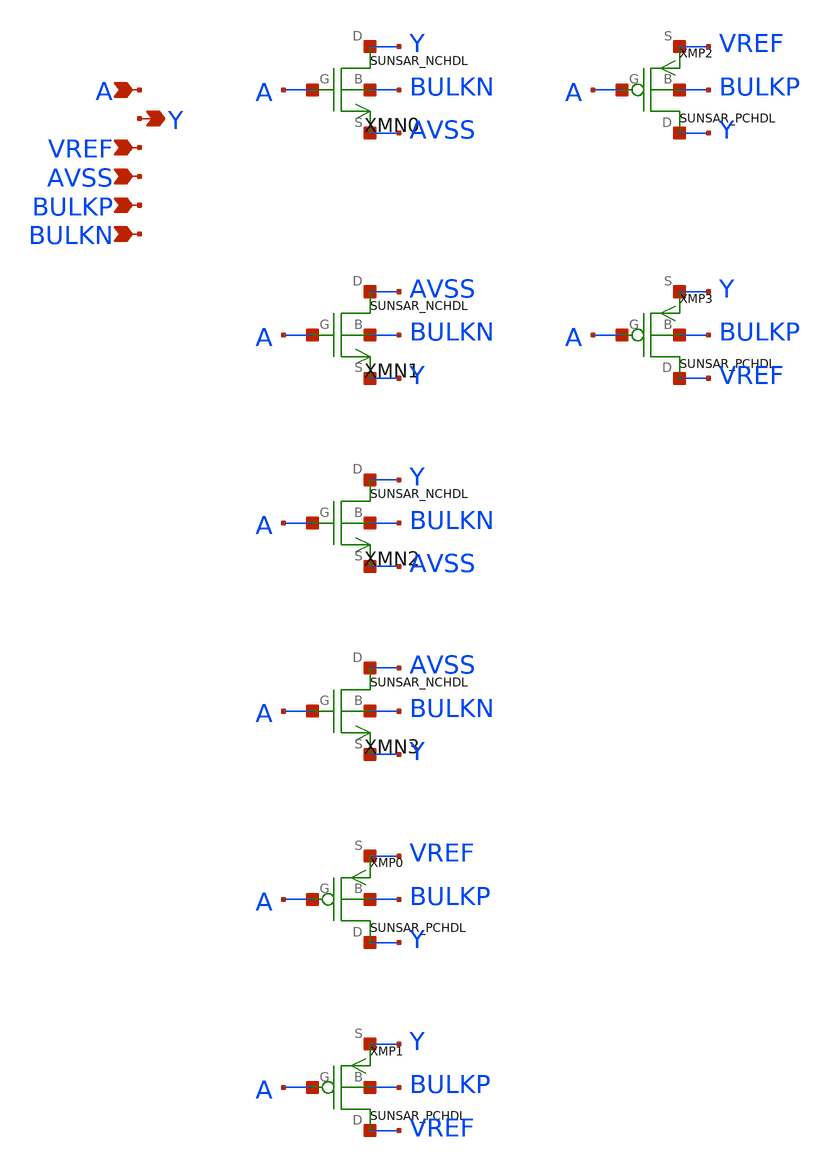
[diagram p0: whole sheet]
** sch_path: ip/sun_sar9b_sky130nm/design/SUN_SAR9B_SKY130NM/SUNSAR_SWX4_CV.sch
**.subckt SUNSAR_SWX4_CV A Y VREF AVSS BULKP BULKN
*.ipin A
*.opin Y
*.ipin VREF
*.ipin AVSS
*.ipin BULKP
*.ipin BULKN
XMN0 Y A AVSS BULKN SUNSAR_NCHDL
XMN1 AVSS A Y BULKN SUNSAR_NCHDL
XMN2 Y A AVSS BULKN SUNSAR_NCHDL
XMN3 AVSS A Y BULKN SUNSAR_NCHDL
XMP0 Y A VREF BULKP SUNSAR_PCHDL
XMP1 VREF A Y BULKP SUNSAR_PCHDL
XMP2 Y A VREF BULKP SUNSAR_PCHDL
XMP3 VREF A Y BULKP SUNSAR_PCHDL
**.ends
.end
